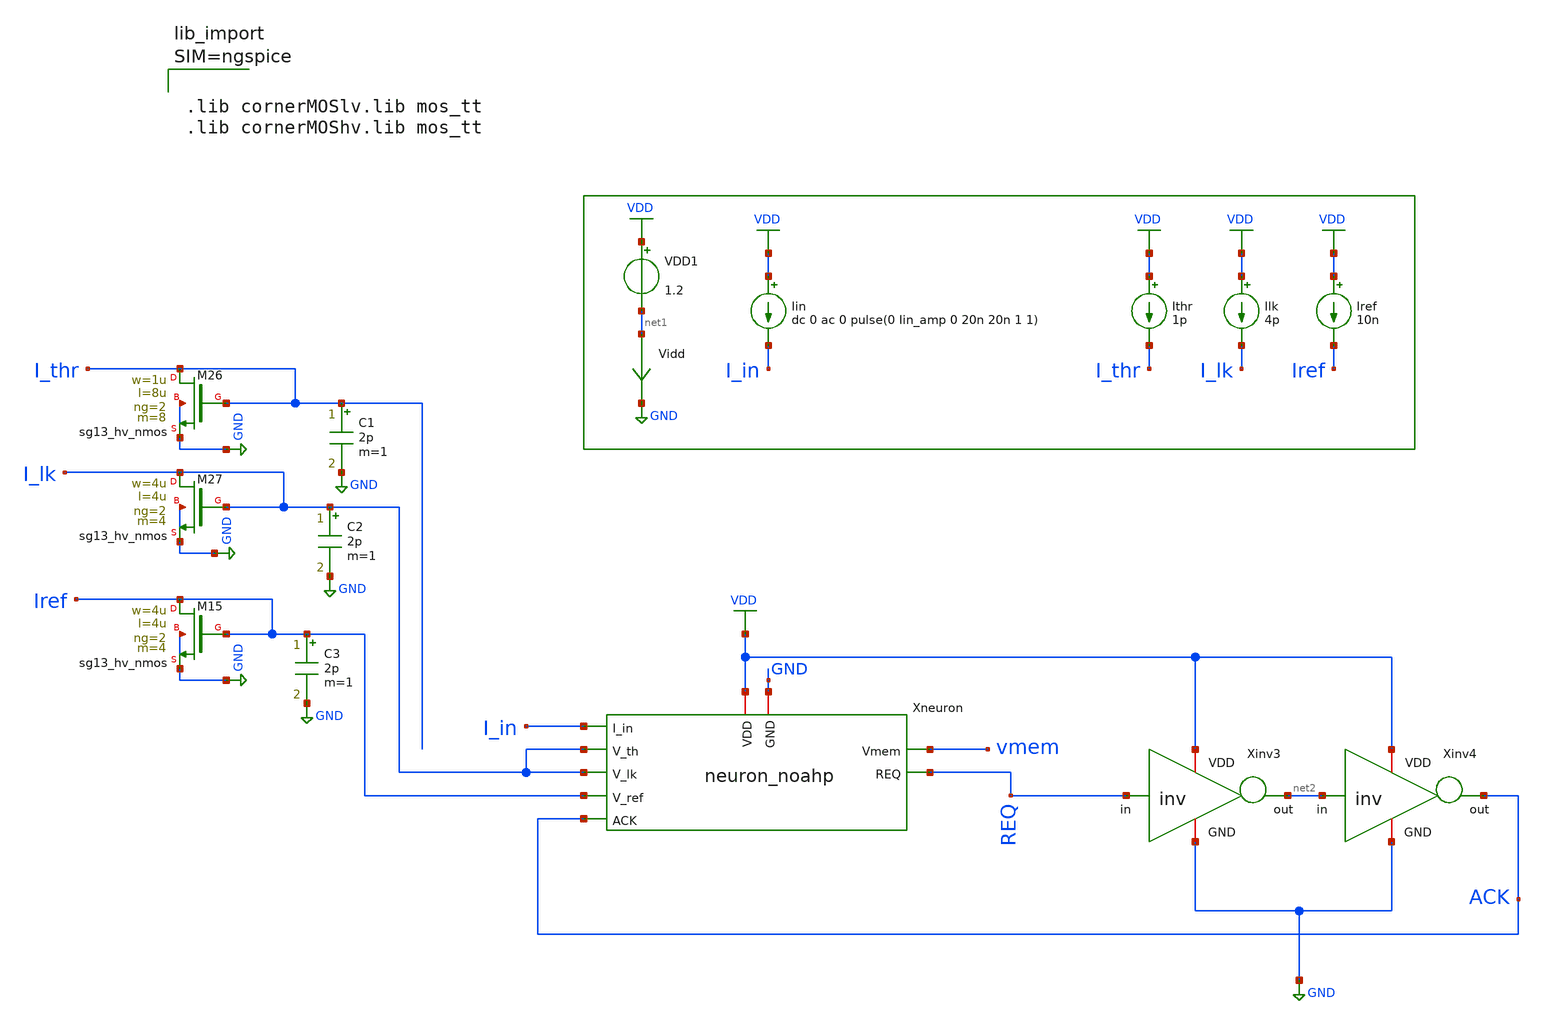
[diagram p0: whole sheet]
** sch_path: xschem/neuron_noahp_tb.sch
**.subckt neuron_noahp_tb
Xneuron VDD I_in I_lk I_lk vmem REQ ACK Iref GND neuron_noahp
Ithr VDD I_thr 1p
Ilk VDD I_lk 4p
Iin VDD I_in dc 0 ac 0 pulse(0 Iin_amp 0 20n 20n 1 1)
VDD1 VDD net1 1.2
Iref VDD Iref 10n
Vidd net1 GND 0
.save i(vidd)
XM26 I_thr I_thr GND GND sg13_hv_nmos w=1u l=8u ng=2 m=8 mm_ok=1
XM27 I_lk I_lk GND GND sg13_hv_nmos w=4u l=4u ng=2 m=4 mm_ok=1
XM15 Iref Iref GND GND sg13_hv_nmos w=4u l=4u ng=2 m=4 mm_ok=1
Xinv3 VDD REQ net2 GND inv
Xinv4 VDD net2 ACK GND inv
C1 I_thr GND 2p m=1
C2 I_lk GND 2p m=1
C3 Iref GND 2p m=1
**** begin user architecture code



.param temp=27
.param Iin_amp=200p

.ic V(vmem)=0 V(xneuron.xref.vref)=0 V(REQ)=0 V(ACK)=0 V(CapAdap)=0

.options gmin=1e-13
.control



* ======================================================
*  Iin sweep - measure firing rate of V(REQ) vs Iin
* ======================================================
*  For each DC value of Iin a transient simulation is run.
*  Rising-edge crossings of V(REQ) through a threshold
*  are counted after a settling window and the firing
*  frequency is computed.  Results go to neuron_iin_sweep.raw
* ======================================================

* --- Sweep parameters (Amps) - edit as needed ---
let iin_start = 0
let iin_stop  = 4000e-12
let iin_step  = 200e-12

* --- Compute number of sweep points ---
let num_pts = (iin_stop - iin_start) / iin_step + 1

* --- Create a new plot to hold the accumulated results ---
setplot new
set resplot = $curplot
let iin_values   = unitvec(num_pts)
let firing_rates = unitvec(num_pts)
let sweep_idx = 0
set t_sim = 50m

* --- Main sweep loop ---
dowhile sweep_idx < num_pts

  * Compute cur_iin fresh each iteration to avoid float drift
  let cur_iin = iin_start + sweep_idx * iin_step

  echo
  echo ============================================
  echo   Sweep point: Iin = $&cur_iin A
  echo ============================================

  * Save cur_iin to a shell variable before tran changes the plot context
  set cur_iin_val = $&cur_iin

  * Set the Iin_amp parameter to the current sweep value.
  alterparam Iin_amp = $cur_iin_val
  reset

  save V(REQ)

  * Run transient analysis with adaptive time
  echo   t_sim = $t_sim
  tran 50n $t_sim

  * --- Measure firing frequency using meas tran ---
  * Skip 1st spike (startup glitch), use 2nd-4th spikes
  let t_rise2 = 0
  let t_rise3 = 0
  let t_rise4 = 0
  meas tran t_rise2 WHEN v(REQ)=0.6 RISE=2
  meas tran t_rise3 WHEN v(REQ)=0.6 RISE=3
  meas tran t_rise4 WHEN v(REQ)=0.6 RISE=4

  * Use best available data for frequency
  if t_rise4 > 0
    * 4+ spikes: use 3rd-4th ISI
    let f_rate = 1.0 / (t_rise4 - t_rise3)
  else
    if t_rise3 > 0
      * 3 spikes: use 2nd-3rd ISI
      let f_rate = 1.0 / (t_rise3 - t_rise2)
    else
      if t_rise2 > 0
        * 2 spikes: estimate rate from time to 2nd spike
        let f_rate = 1.0 / t_rise2
      else
        * No real spikes (only glitch or none)
        let f_rate = 0
      end
    end
  end

  echo   freq = $&f_rate Hz

  * --- Update t_sim for next sweep point ---
  * Need ~5 spikes worth of time, clamp to [1ms, 50ms]
  if f_rate > 0
    let t_next = 5.0 / f_rate
    if t_next < 1e-3
      let t_next = 1e-3
    end
    if t_next > 50e-3
      let t_next = 50e-3
    end
    set t_sim = $&t_next
  end

  * --- Store this point's results in the result plot ---
  set save_freq = $&f_rate
  setplot $resplot
  let iin_values[sweep_idx]   = $cur_iin_val
  let firing_rates[sweep_idx] = $save_freq
  let sweep_idx = sweep_idx + 1

end

* --- Write the result vectors to a .raw file ---
setplot $resplot
write neuron_iin_sweep.raw iin_values firing_rates

echo
echo ============================================
echo   Iin sweep complete!
echo   Results saved to:  neuron_iin_sweep.raw
echo   Vectors:
echo     iin_values   (A)  - input current
echo     firing_rates (Hz) - neuron firing rate
echo ============================================

.endc







.lib cornerMOSlv.lib mos_tt
.lib cornerMOShv.lib mos_tt


**** end user architecture code
**.ends

* expanding   symbol:  neuron_noahp.sym # of pins=9
** sym_path: xschem/neuron_noahp.sym
** sch_path: xschem/neuron_noahp.sch
.subckt neuron_noahp VDD I_in V_th V_lk Vmem REQ ACK V_ref GND
*.ipin V_ref
*.iopin GND
*.iopin VDD
*.opin REQ
*.ipin ACK
*.ipin I_in
*.ipin V_th
*.ipin V_lk
*.opin Vmem
Xinv1 VDD Vfb net1 GND inv
Xinv2 VDD net1 REQ GND inv
Xdpi1 I_in VDD V_th Vmem V_lk GND DPI
Xfb VDD Vfb Vmem GND FB_system
Xref VDD ACK Vmem REQ V_ref GND REF_system
Cmem Vmem GND 1p m=1
.ends


* expanding   symbol:  inv.sym # of pins=4
** sym_path: xschem/inv.sym
** sch_path: xschem/inv.sch
.subckt inv VDD in out GND
*.ipin in
*.iopin VDD
*.iopin GND
*.opin out
XM1 out in VDD VDD sg13_hv_pmos w=1u l=0.5u ng=1 m=1 mm_ok=1
XM2 out in GND GND sg13_hv_nmos w=1u l=0.5u ng=1 m=1 mm_ok=1
.ends


* expanding   symbol:  DPI.sym # of pins=6
** sym_path: xschem/DPI.sym
** sch_path: xschem/DPI.sch
.subckt DPI I_in VDD V_th V_mem V_lk GND
*.opin V_mem
*.ipin V_lk
*.ipin V_th
*.ipin I_in
*.iopin VDD
*.iopin GND
XMdifl GND V_th I_in VDD sg13_hv_pmos w=4u l=2u ng=2 m=8 mm_ok=1
XMdifr V_mem V_mem I_in VDD sg13_hv_pmos w=4u l=2u ng=2 m=8 mm_ok=1
XMtau net1 V_lk GND GND sg13_hv_nmos w=4u l=4u ng=2 m=4 mm_ok=1
Vilk V_mem net1 0
.save i(vilk)
.ends


* expanding   symbol:  FB_system.sym # of pins=4
** sym_path: FB_system.sym
** sch_path: FB_system.sch
.subckt FB_system VDD out V_mem GND
*.opin out
*.iopin V_mem
*.iopin VDD
*.iopin GND
XMmirr Vmir Vmir VDD VDD sg13_hv_pmos w=4u l=2u ng=4 m=1 mm_ok=1
XMfbsw V_mem out net1 VDD sg13_hv_pmos w=1u l=0.5u ng=2 m=1 mm_ok=1
XMmirl4 net1 Vmir net2 VDD sg13_hv_pmos w=1u l=2u ng=1 m=1 mm_ok=1
XMthr out V_mem Vmir VDD sg13_hv_pmos w=1u l=2u ng=2 m=4 mm_ok=1
XMmem1 out V_mem net3 GND sg13_hv_nmos w=1u l=2u ng=1 m=2 mm_ok=1
XMmirl3 net2 Vmir net4 VDD sg13_hv_pmos w=1u l=2u ng=1 m=1 mm_ok=1
XMmirl2 net4 Vmir net5 VDD sg13_hv_pmos w=1u l=2u ng=1 m=1 mm_ok=1
XMmirl1 net5 Vmir VDD VDD sg13_hv_pmos w=1u l=2u ng=1 m=1 mm_ok=1
XMmem2 net3 V_mem net6 GND sg13_hv_nmos w=1u l=2u ng=1 m=2 mm_ok=1
XMmem3 net6 V_mem net7 GND sg13_hv_nmos w=1u l=2u ng=1 m=2 mm_ok=1
XMmem4 net7 V_mem GND GND sg13_hv_nmos w=1u l=2u ng=1 m=2 mm_ok=1
.ends


* expanding   symbol:  REF_system.sym # of pins=6
** sym_path: xschem/REF_system.sym
** sch_path: xschem/REF_system.sch
.subckt REF_system VDD ACK V_mem REQ V_ref GND
*.iopin VDD
*.iopin GND
*.ipin V_ref
*.ipin REQ
*.ipin ACK
*.ipin V_mem
Cr Vref GND 0.5p m=1
XM10 Vref REQ net2 VDD sg13_hv_pmos w=1u l=0.5u ng=1 m=1 mm_ok=1
XM11 Vref REQ net1 GND sg13_hv_nmos w=1u l=0.5u ng=1 m=1 mm_ok=1
XM12 net2 ACK VDD VDD sg13_hv_pmos w=1u l=0.5u ng=1 m=1 mm_ok=1
XM13 V_mem Vref GND GND sg13_hv_nmos w=1u l=0.5u ng=1 m=1 mm_ok=1
XM14 net1 V_ref GND GND sg13_hv_nmos w=4u l=4u ng=2 m=4 mm_ok=1
.ends

.GLOBAL GND
.GLOBAL VDD
.end
